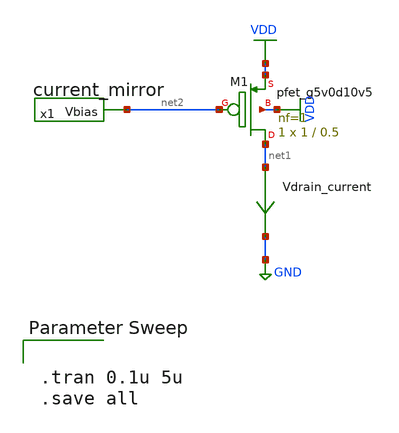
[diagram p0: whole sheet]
** sch_path: Abishek_Sam_group/test_current_mirror.sch
**.subckt test_current_mirror
x1 net2 current_mirror
XM1 net1 net2 VDD VDD sky130_fd_pr__pfet_g5v0d10v5 L=0.5 W=1 nf=1 ad='int((nf+1)/2) * W/nf * 0.29' as='int((nf+2)/2) * W/nf * 0.29'
+ pd='2*int((nf+1)/2) * (W/nf + 0.29)' ps='2*int((nf+2)/2) * (W/nf + 0.29)' nrd='0.29 / W' nrs='0.29 / W'
+ sa=0 sb=0 sd=0 mult=1 m=1
Vdrain_current net1 GND 0
.save i(vdrain_current)
**** begin user architecture code

.lib $::SKYWATER_MODELS/sky130.lib.spice tt



.tran 0.1u 5u
.save all


**** end user architecture code
**.ends

* expanding   symbol:  current_mirror.sym # of pins=1
** sym_path: Abishek_Sam_group/template/current_mirror.sym
** sch_path: Abishek_Sam_group/template/current_mirror.sch
.subckt current_mirror Vbias
*.opin Vbias
XM1 Vbias Vbias VDD VDD sky130_fd_pr__pfet_g5v0d10v5 L=0.5 W=2 nf=1 ad='int((nf+1)/2) * W/nf * 0.29'
+ as='int((nf+2)/2) * W/nf * 0.29' pd='2*int((nf+1)/2) * (W/nf + 0.29)' ps='2*int((nf+2)/2) * (W/nf + 0.29)'
+ nrd='0.29 / W' nrs='0.29 / W' sa=0 sb=0 sd=0 mult=1 m=1
I0 Vbias GND 3u
.ends

.GLOBAL VDD
.GLOBAL GND
.end
